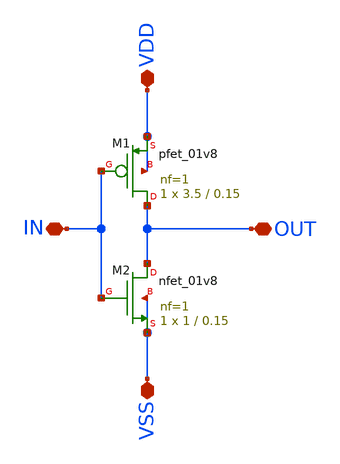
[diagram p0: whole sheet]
** sch_path: design/xschem/inv.sch
**.subckt inv VDD VSS IN OUT
*.iopin VDD
*.iopin VSS
*.iopin IN
*.iopin OUT
XM1 OUT IN VDD VDD sky130_fd_pr__pfet_01v8 L=0.15 W=3.5 nf=1 ad='int((nf+1)/2) * W/nf * 0.29' as='int((nf+2)/2) * W/nf * 0.29'
+ pd='2*int((nf+1)/2) * (W/nf + 0.29)' ps='2*int((nf+2)/2) * (W/nf + 0.29)' nrd='0.29 / W' nrs='0.29 / W'
+ sa=0 sb=0 sd=0 mult=1 m=1
XM2 OUT IN VSS VSS sky130_fd_pr__nfet_01v8 L=0.15 W=1 nf=1 ad='int((nf+1)/2) * W/nf * 0.29' as='int((nf+2)/2) * W/nf * 0.29'
+ pd='2*int((nf+1)/2) * (W/nf + 0.29)' ps='2*int((nf+2)/2) * (W/nf + 0.29)' nrd='0.29 / W' nrs='0.29 / W'
+ sa=0 sb=0 sd=0 mult=1 m=1
**.ends
.end
